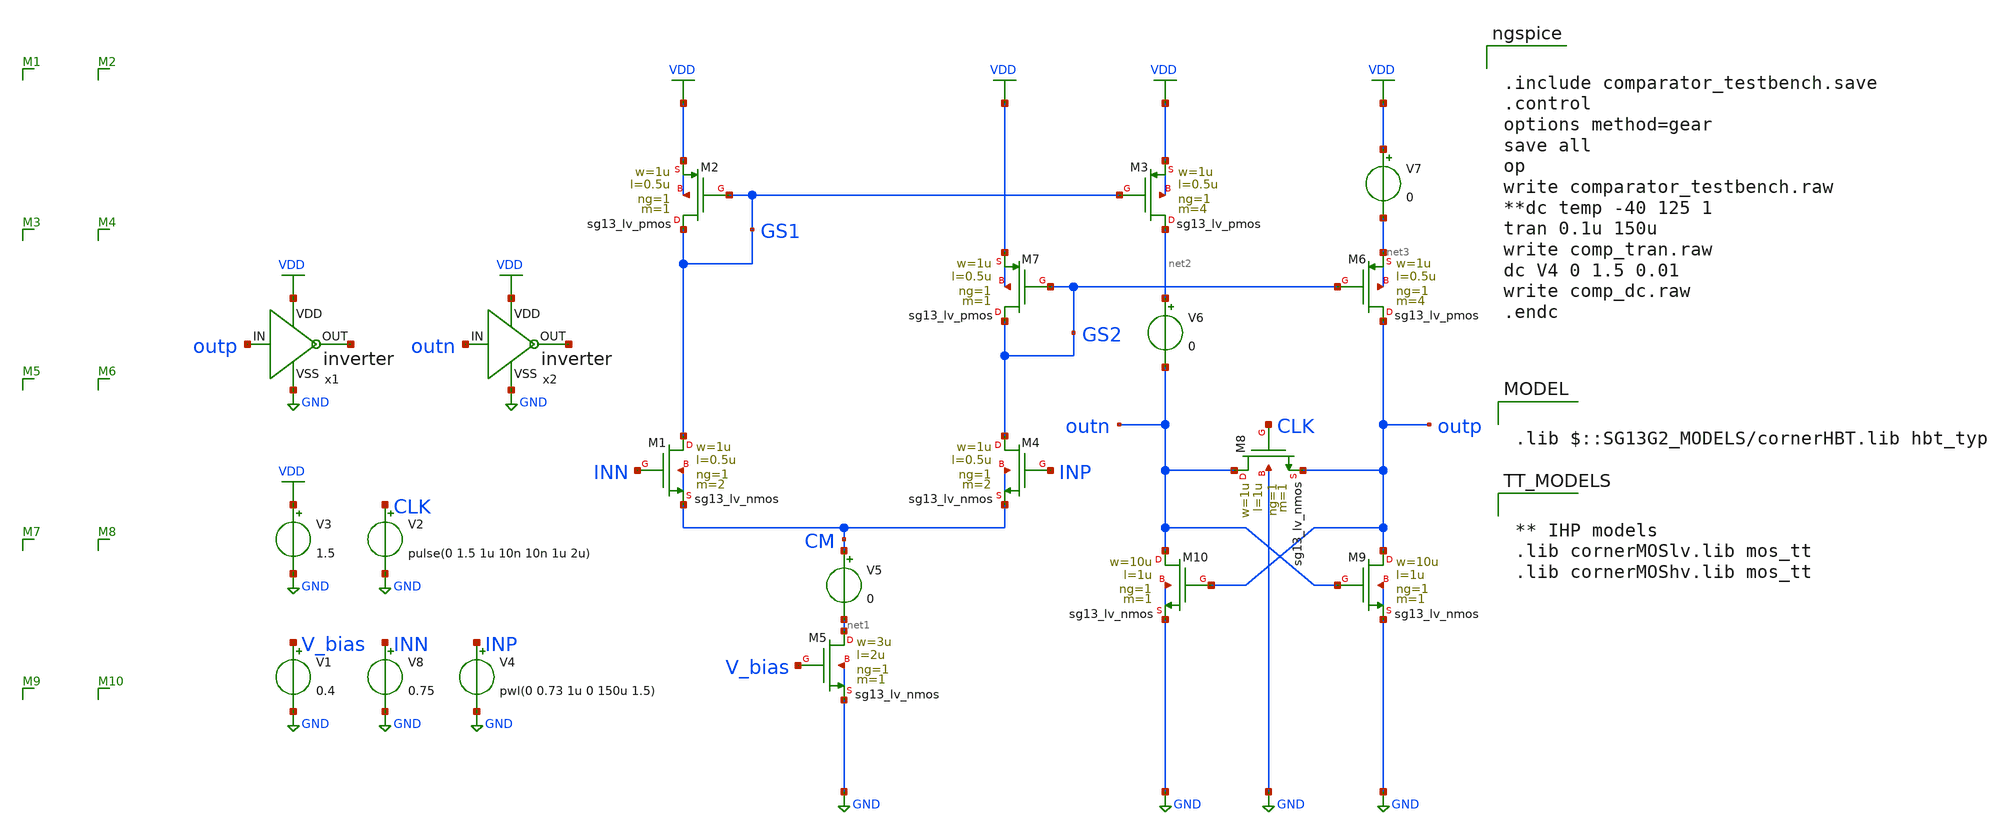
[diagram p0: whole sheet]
** sch_path: 00-testbenches/comparator_testbench.sch
**.subckt comparator_testbench
XM1 GS1 INN CM CM sg13_lv_nmos w=1u l=0.5u ng=1 m=2 mm_ok=1
XM2 GS1 GS1 VDD VDD sg13_lv_pmos w=1u l=0.5u ng=1 m=1 mm_ok=1
XM3 net2 GS1 VDD VDD sg13_lv_pmos w=1u l=0.5u ng=1 m=4 mm_ok=1
XM4 GS2 INP CM CM sg13_lv_nmos w=1u l=0.5u ng=1 m=2 mm_ok=1
XM5 net1 V_bias GND GND sg13_lv_nmos w=3u l=2u ng=1 m=1 mm_ok=1
XM7 GS2 GS2 VDD VDD sg13_lv_pmos w=1u l=0.5u ng=1 m=1 mm_ok=1
XM6 outp GS2 net3 net3 sg13_lv_pmos w=1u l=0.5u ng=1 m=4 mm_ok=1
XM8 outn CLK outp GND sg13_lv_nmos w=1u l=1u ng=1 m=1 mm_ok=1
XM9 outp outn GND GND sg13_lv_nmos w=10u l=1u ng=1 m=1 mm_ok=1
XM10 outn outp GND GND sg13_lv_nmos w=10u l=1u ng=1 m=1 mm_ok=1
V1 V_bias GND 0.4
V3 VDD GND 1.5
V4 INP GND pwl(0 0.73 1u 0 150u 1.5)
V5 CM net1 0
V6 net2 outn 0
V7 VDD net3 0
V2 CLK GND pulse(0 1.5 1u 10n 10n 1u 2u)
V8 INN GND 0.75
x1 VDD outp net4 GND inverter
x2 VDD outn net5 GND inverter
**** begin user architecture code


.include comparator_testbench.save
.control
options method=gear
save all
op
write comparator_testbench.raw
**dc temp -40 125 1
tran 0.1u 150u
write comp_tran.raw
dc V4 0 1.5 0.01
write comp_dc.raw
.endc




** IHP models
.lib cornerMOSlv.lib mos_tt
.lib cornerMOShv.lib mos_tt



.lib $::SG13G2_MODELS/cornerHBT.lib hbt_typ

**** end user architecture code
**.ends
.GLOBAL VDD
.GLOBAL GND
.end
